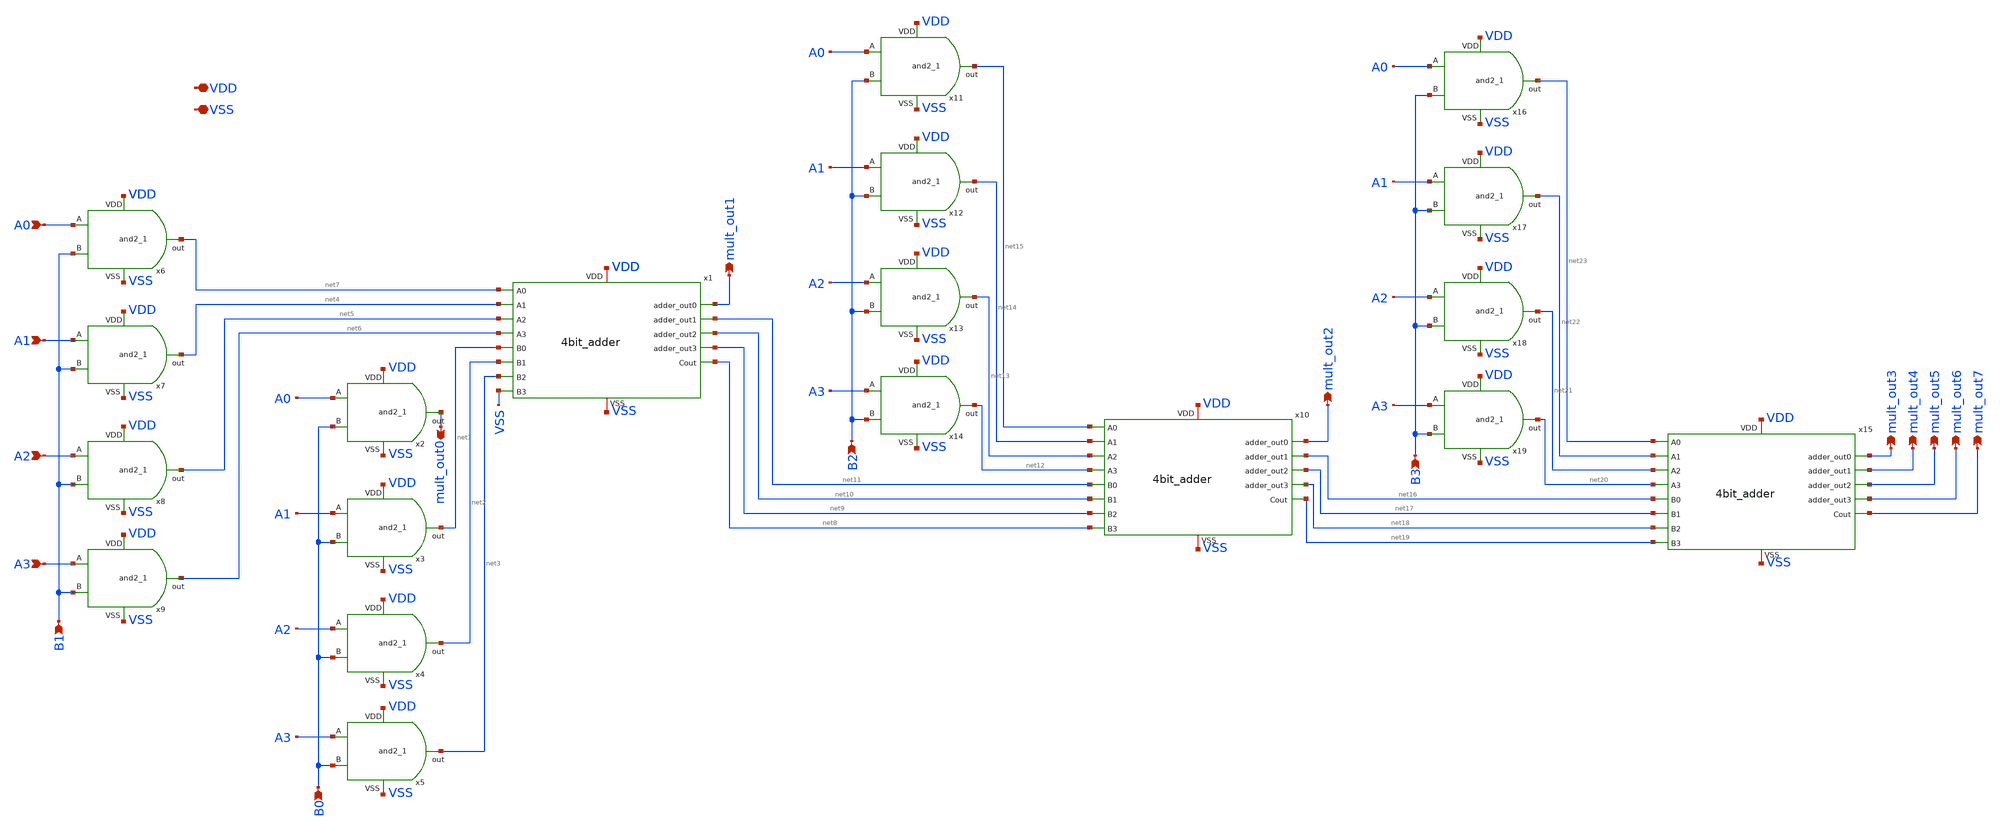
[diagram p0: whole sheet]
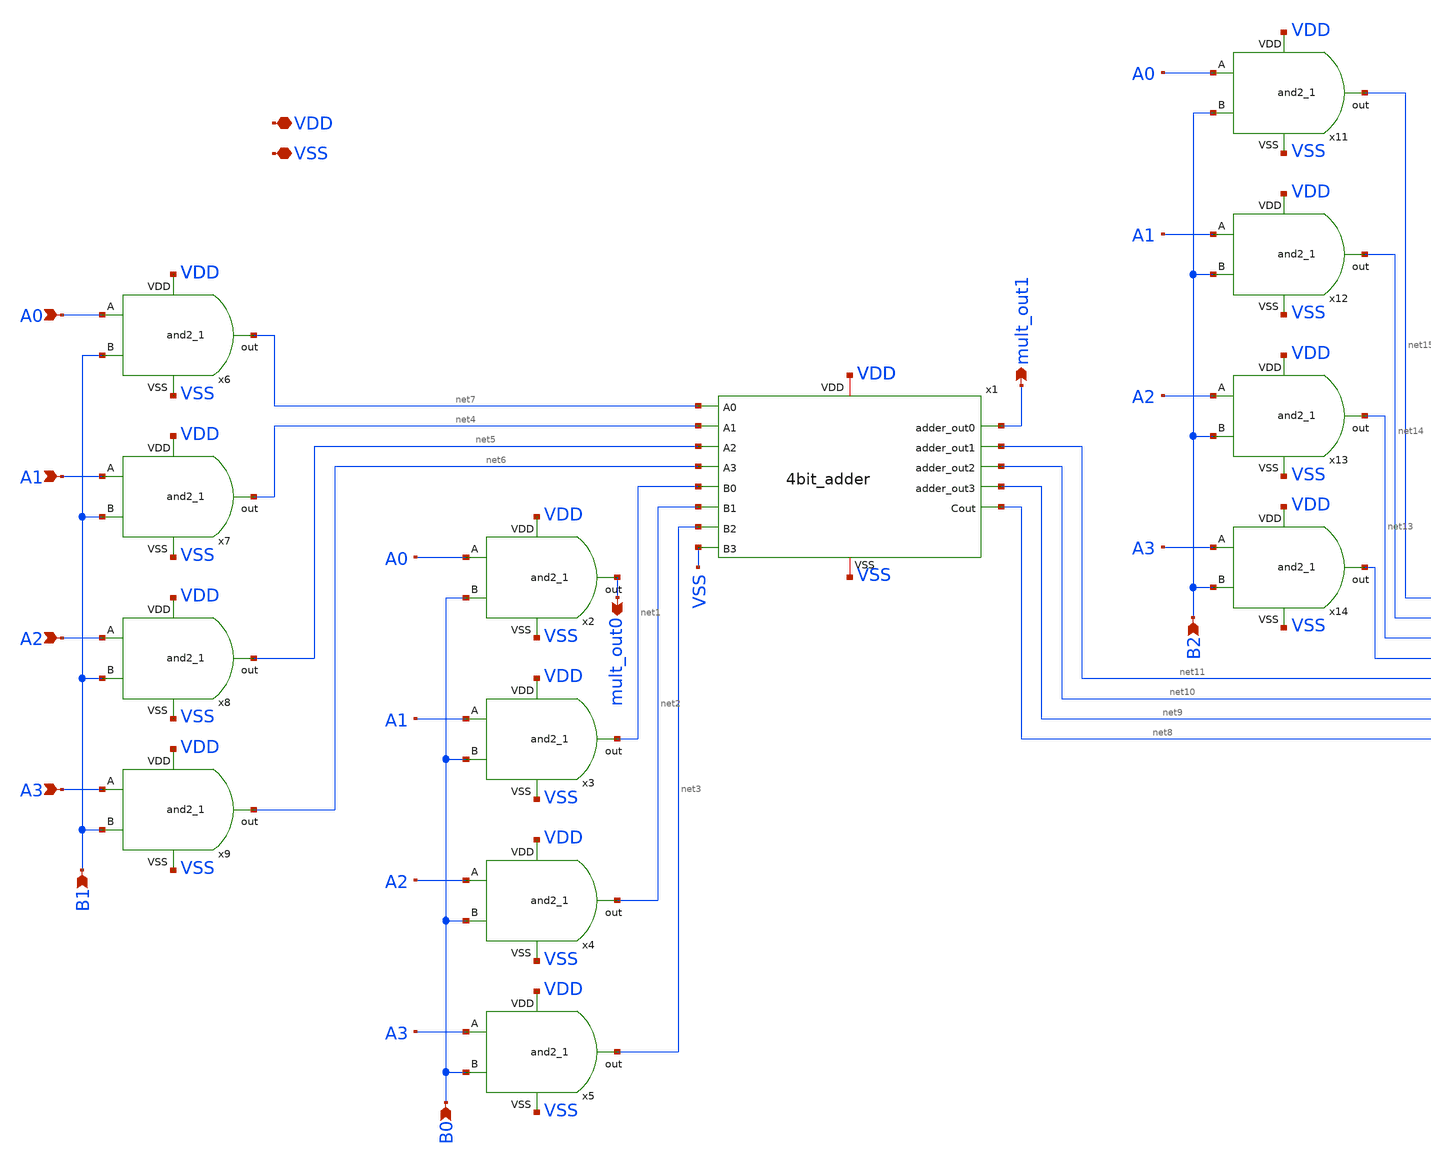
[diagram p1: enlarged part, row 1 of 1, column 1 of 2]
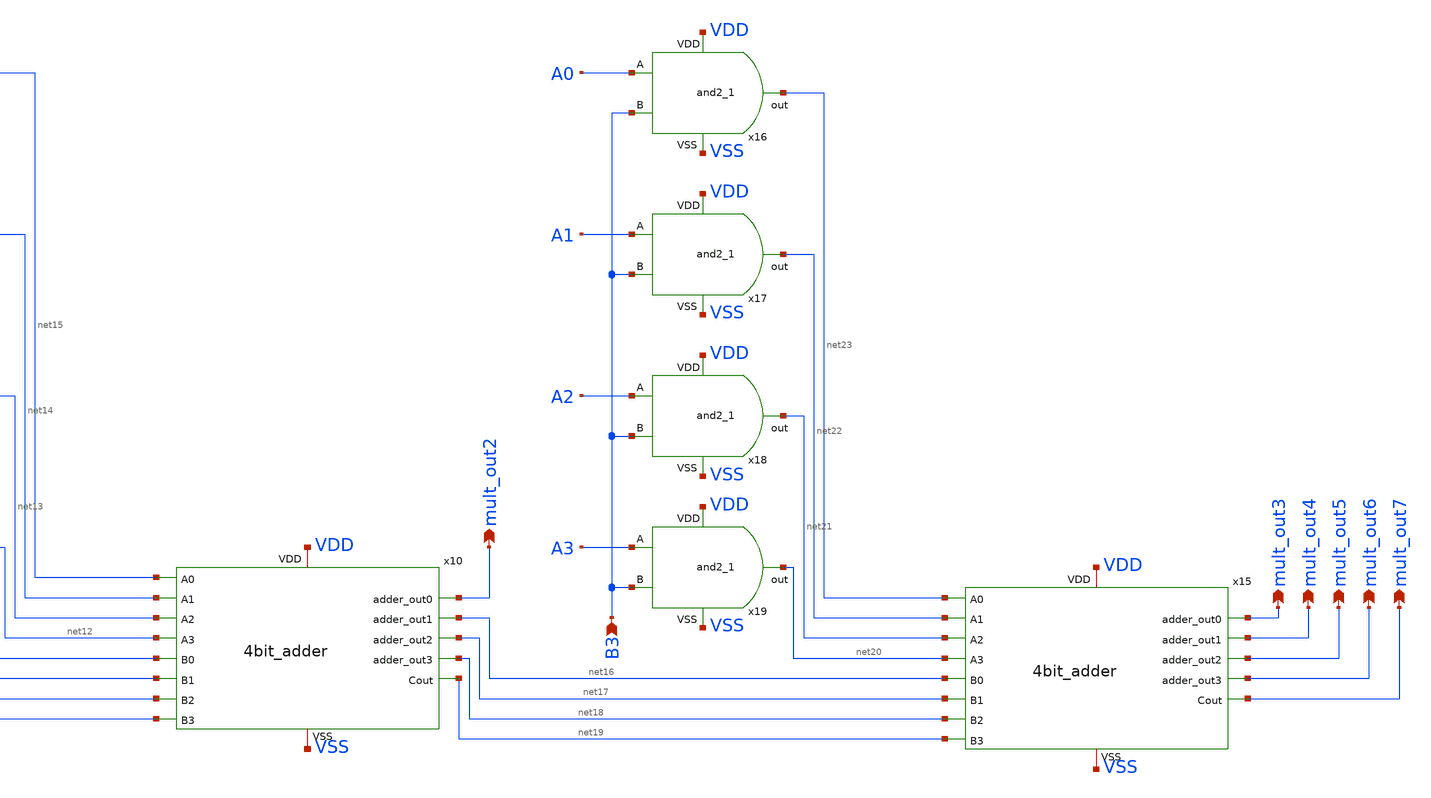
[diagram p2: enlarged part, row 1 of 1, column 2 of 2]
** sch_path: 8bit_multiplier.sch
**.subckt 8bit_multiplier VDD VSS A0 A1 A2 A3 B1 mult_out0 B0 mult_out1 B2 B3 mult_out2 mult_out3
*+ mult_out4 mult_out5 mult_out6 mult_out7
*.iopin VDD
*.iopin VSS
*.ipin A0
*.ipin A1
*.ipin A2
*.ipin A3
*.ipin B1
*.opin mult_out0
*.ipin B0
*.opin mult_out1
*.ipin B2
*.ipin B3
*.opin mult_out2
*.opin mult_out3
*.opin mult_out4
*.opin mult_out5
*.opin mult_out6
*.opin mult_out7
x1 VDD VSS net9 net10 net11 mult_out1 net7 net1 net8 VSS net6 net3 net4 net5 net2 4bit_adder
x2 VSS VDD A0 mult_out0 B0 and2
x3 VSS VDD A1 net1 B0 and2
x4 VSS VDD A2 net2 B0 and2
x5 VSS VDD A3 net3 B0 and2
x6 VSS VDD A0 net7 B1 and2
x7 VSS VDD A1 net4 B1 and2
x8 VSS VDD A2 net5 B1 and2
x9 VSS VDD A3 net6 B1 and2
x10 VDD VSS net18 net17 net16 mult_out2 net15 net11 net19 net8 net12 net9 net14 net13 net10
+ 4bit_adder
x11 VSS VDD A0 net15 B2 and2
x12 VSS VDD A1 net14 B2 and2
x13 VSS VDD A2 net13 B2 and2
x14 VSS VDD A3 net12 B2 and2
x15 VDD VSS mult_out6 mult_out5 mult_out4 mult_out3 net23 net16 mult_out7 net19 net20 net18 net22
+ net21 net17 4bit_adder
x16 VSS VDD A0 net23 B3 and2
x17 VSS VDD A1 net22 B3 and2
x18 VSS VDD A2 net21 B3 and2
x19 VSS VDD A3 net20 B3 and2
**.ends
.end
